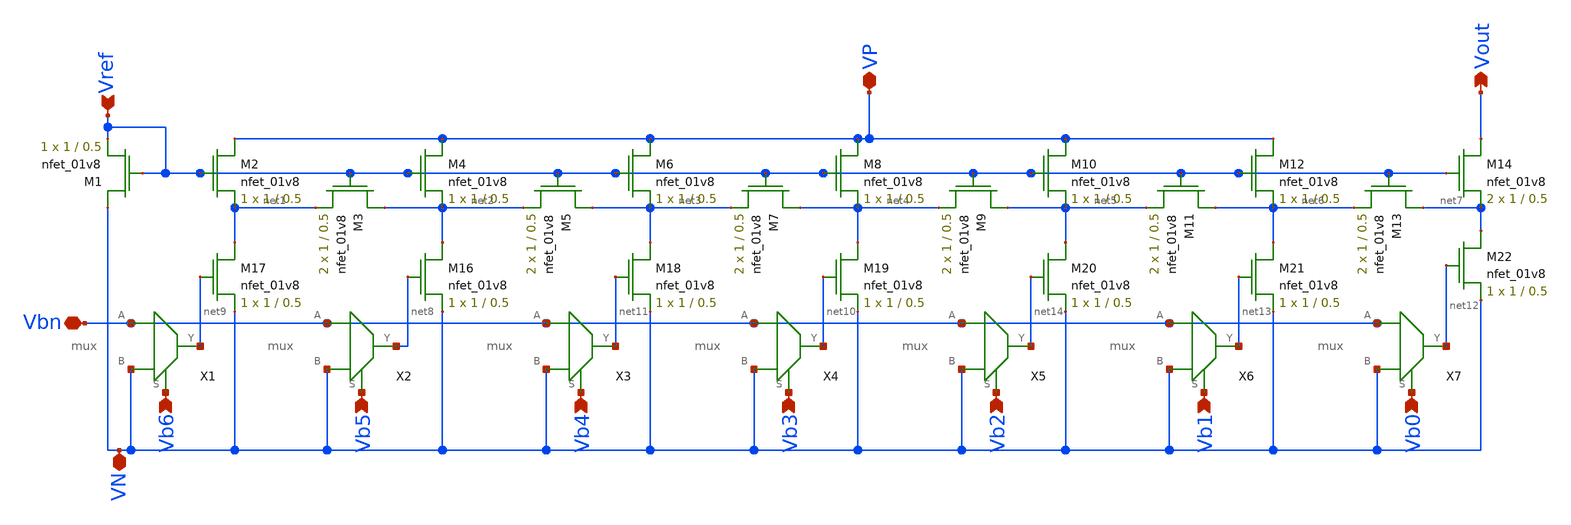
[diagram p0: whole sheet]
** sch_path: dac/schematics/misc/dac.sch
**.subckt dac VN VP Vout Vref Vb6 Vb5 Vb4 Vb3 Vb2 Vb1 Vb0 Vbn
*.iopin VN
*.iopin VP
*.opin Vout
*.ipin Vref
*.ipin Vb6
*.ipin Vb5
*.ipin Vb4
*.ipin Vb3
*.ipin Vb2
*.ipin Vb1
*.ipin Vb0
*.iopin Vbn
XM1 VN Vref Vref GND sky130_fd_pr__nfet_01v8 L=0.5 W=1 nf=1 ad='int((nf+1)/2) * W/nf * 0.29' as='int((nf+2)/2) * W/nf * 0.29'
+ pd='2*int((nf+1)/2) * (W/nf + 0.29)' ps='2*int((nf+2)/2) * (W/nf + 0.29)' nrd='0.29 / W' nrs='0.29 / W'
+ sa=0 sb=0 sd=0 mult=1 m=1
XM3 net2 Vref net1 GND sky130_fd_pr__nfet_01v8 L=0.5 W=1 nf=1 ad='int((nf+1)/2) * W/nf * 0.29' as='int((nf+2)/2) * W/nf * 0.29'
+ pd='2*int((nf+1)/2) * (W/nf + 0.29)' ps='2*int((nf+2)/2) * (W/nf + 0.29)' nrd='0.29 / W' nrs='0.29 / W'
+ sa=0 sb=0 sd=0 mult=2 m=2
XM2 VP Vref net1 GND sky130_fd_pr__nfet_01v8 L=0.5 W=1 nf=1 ad='int((nf+1)/2) * W/nf * 0.29' as='int((nf+2)/2) * W/nf * 0.29'
+ pd='2*int((nf+1)/2) * (W/nf + 0.29)' ps='2*int((nf+2)/2) * (W/nf + 0.29)' nrd='0.29 / W' nrs='0.29 / W'
+ sa=0 sb=0 sd=0 mult=1 m=1
XM4 VP Vref net2 GND sky130_fd_pr__nfet_01v8 L=0.5 W=1 nf=1 ad='int((nf+1)/2) * W/nf * 0.29' as='int((nf+2)/2) * W/nf * 0.29'
+ pd='2*int((nf+1)/2) * (W/nf + 0.29)' ps='2*int((nf+2)/2) * (W/nf + 0.29)' nrd='0.29 / W' nrs='0.29 / W'
+ sa=0 sb=0 sd=0 mult=1 m=1
XM6 VP Vref net3 GND sky130_fd_pr__nfet_01v8 L=0.5 W=1 nf=1 ad='int((nf+1)/2) * W/nf * 0.29' as='int((nf+2)/2) * W/nf * 0.29'
+ pd='2*int((nf+1)/2) * (W/nf + 0.29)' ps='2*int((nf+2)/2) * (W/nf + 0.29)' nrd='0.29 / W' nrs='0.29 / W'
+ sa=0 sb=0 sd=0 mult=1 m=1
XM8 VP Vref net4 GND sky130_fd_pr__nfet_01v8 L=0.5 W=1 nf=1 ad='int((nf+1)/2) * W/nf * 0.29' as='int((nf+2)/2) * W/nf * 0.29'
+ pd='2*int((nf+1)/2) * (W/nf + 0.29)' ps='2*int((nf+2)/2) * (W/nf + 0.29)' nrd='0.29 / W' nrs='0.29 / W'
+ sa=0 sb=0 sd=0 mult=1 m=1
XM10 VP Vref net5 GND sky130_fd_pr__nfet_01v8 L=0.5 W=1 nf=1 ad='int((nf+1)/2) * W/nf * 0.29' as='int((nf+2)/2) * W/nf * 0.29'
+ pd='2*int((nf+1)/2) * (W/nf + 0.29)' ps='2*int((nf+2)/2) * (W/nf + 0.29)' nrd='0.29 / W' nrs='0.29 / W'
+ sa=0 sb=0 sd=0 mult=1 m=1
XM12 VP Vref net6 GND sky130_fd_pr__nfet_01v8 L=0.5 W=1 nf=1 ad='int((nf+1)/2) * W/nf * 0.29' as='int((nf+2)/2) * W/nf * 0.29'
+ pd='2*int((nf+1)/2) * (W/nf + 0.29)' ps='2*int((nf+2)/2) * (W/nf + 0.29)' nrd='0.29 / W' nrs='0.29 / W'
+ sa=0 sb=0 sd=0 mult=1 m=1
XM14 Vout Vref net7 GND sky130_fd_pr__nfet_01v8 L=0.5 W=1 nf=1 ad='int((nf+1)/2) * W/nf * 0.29' as='int((nf+2)/2) * W/nf * 0.29'
+ pd='2*int((nf+1)/2) * (W/nf + 0.29)' ps='2*int((nf+2)/2) * (W/nf + 0.29)' nrd='0.29 / W' nrs='0.29 / W'
+ sa=0 sb=0 sd=0 mult=2 m=2
XM5 net3 Vref net2 GND sky130_fd_pr__nfet_01v8 L=0.5 W=1 nf=1 ad='int((nf+1)/2) * W/nf * 0.29' as='int((nf+2)/2) * W/nf * 0.29'
+ pd='2*int((nf+1)/2) * (W/nf + 0.29)' ps='2*int((nf+2)/2) * (W/nf + 0.29)' nrd='0.29 / W' nrs='0.29 / W'
+ sa=0 sb=0 sd=0 mult=2 m=2
XM7 net4 Vref net3 GND sky130_fd_pr__nfet_01v8 L=0.5 W=1 nf=1 ad='int((nf+1)/2) * W/nf * 0.29' as='int((nf+2)/2) * W/nf * 0.29'
+ pd='2*int((nf+1)/2) * (W/nf + 0.29)' ps='2*int((nf+2)/2) * (W/nf + 0.29)' nrd='0.29 / W' nrs='0.29 / W'
+ sa=0 sb=0 sd=0 mult=2 m=2
XM9 net5 Vref net4 GND sky130_fd_pr__nfet_01v8 L=0.5 W=1 nf=1 ad='int((nf+1)/2) * W/nf * 0.29' as='int((nf+2)/2) * W/nf * 0.29'
+ pd='2*int((nf+1)/2) * (W/nf + 0.29)' ps='2*int((nf+2)/2) * (W/nf + 0.29)' nrd='0.29 / W' nrs='0.29 / W'
+ sa=0 sb=0 sd=0 mult=2 m=2
XM11 net6 Vref net5 GND sky130_fd_pr__nfet_01v8 L=0.5 W=1 nf=1 ad='int((nf+1)/2) * W/nf * 0.29' as='int((nf+2)/2) * W/nf * 0.29'
+ pd='2*int((nf+1)/2) * (W/nf + 0.29)' ps='2*int((nf+2)/2) * (W/nf + 0.29)' nrd='0.29 / W' nrs='0.29 / W'
+ sa=0 sb=0 sd=0 mult=2 m=2
XM13 net7 Vref net6 GND sky130_fd_pr__nfet_01v8 L=0.5 W=1 nf=1 ad='int((nf+1)/2) * W/nf * 0.29' as='int((nf+2)/2) * W/nf * 0.29'
+ pd='2*int((nf+1)/2) * (W/nf + 0.29)' ps='2*int((nf+2)/2) * (W/nf + 0.29)' nrd='0.29 / W' nrs='0.29 / W'
+ sa=0 sb=0 sd=0 mult=2 m=2
XM16 net2 net8 VN GND sky130_fd_pr__nfet_01v8 L=0.5 W=1 nf=1 ad='int((nf+1)/2) * W/nf * 0.29' as='int((nf+2)/2) * W/nf * 0.29'
+ pd='2*int((nf+1)/2) * (W/nf + 0.29)' ps='2*int((nf+2)/2) * (W/nf + 0.29)' nrd='0.29 / W' nrs='0.29 / W'
+ sa=0 sb=0 sd=0 mult=1 m=1
XM17 net1 net9 VN GND sky130_fd_pr__nfet_01v8 L=0.5 W=1 nf=1 ad='int((nf+1)/2) * W/nf * 0.29' as='int((nf+2)/2) * W/nf * 0.29'
+ pd='2*int((nf+1)/2) * (W/nf + 0.29)' ps='2*int((nf+2)/2) * (W/nf + 0.29)' nrd='0.29 / W' nrs='0.29 / W'
+ sa=0 sb=0 sd=0 mult=1 m=1
XM18 net3 net11 VN GND sky130_fd_pr__nfet_01v8 L=0.5 W=1 nf=1 ad='int((nf+1)/2) * W/nf * 0.29' as='int((nf+2)/2) * W/nf * 0.29'
+ pd='2*int((nf+1)/2) * (W/nf + 0.29)' ps='2*int((nf+2)/2) * (W/nf + 0.29)' nrd='0.29 / W' nrs='0.29 / W'
+ sa=0 sb=0 sd=0 mult=1 m=1
XM19 net4 net10 VN GND sky130_fd_pr__nfet_01v8 L=0.5 W=1 nf=1 ad='int((nf+1)/2) * W/nf * 0.29' as='int((nf+2)/2) * W/nf * 0.29'
+ pd='2*int((nf+1)/2) * (W/nf + 0.29)' ps='2*int((nf+2)/2) * (W/nf + 0.29)' nrd='0.29 / W' nrs='0.29 / W'
+ sa=0 sb=0 sd=0 mult=1 m=1
XM20 net5 net14 VN GND sky130_fd_pr__nfet_01v8 L=0.5 W=1 nf=1 ad='int((nf+1)/2) * W/nf * 0.29' as='int((nf+2)/2) * W/nf * 0.29'
+ pd='2*int((nf+1)/2) * (W/nf + 0.29)' ps='2*int((nf+2)/2) * (W/nf + 0.29)' nrd='0.29 / W' nrs='0.29 / W'
+ sa=0 sb=0 sd=0 mult=1 m=1
XM21 net6 net13 VN GND sky130_fd_pr__nfet_01v8 L=0.5 W=1 nf=1 ad='int((nf+1)/2) * W/nf * 0.29' as='int((nf+2)/2) * W/nf * 0.29'
+ pd='2*int((nf+1)/2) * (W/nf + 0.29)' ps='2*int((nf+2)/2) * (W/nf + 0.29)' nrd='0.29 / W' nrs='0.29 / W'
+ sa=0 sb=0 sd=0 mult=1 m=1
XM22 net7 net12 VN GND sky130_fd_pr__nfet_01v8 L=0.5 W=1 nf=1 ad='int((nf+1)/2) * W/nf * 0.29' as='int((nf+2)/2) * W/nf * 0.29'
+ pd='2*int((nf+1)/2) * (W/nf + 0.29)' ps='2*int((nf+2)/2) * (W/nf + 0.29)' nrd='0.29 / W' nrs='0.29 / W'
+ sa=0 sb=0 sd=0 mult=1 m=1
X1 Vbn VN net9 Vb6 mux
X2 Vbn VN net8 Vb5 mux
X3 Vbn VN net11 Vb4 mux
X4 Vbn VN net10 Vb3 mux
X5 Vbn VN net14 Vb2 mux
X6 Vbn VN net13 Vb1 mux
X7 Vbn VN net12 Vb0 mux
**.ends

* expanding   symbol:  /home/madvlsi/current-output-dac-vlsi/schematics/mux.sym # of pins=4
** sym_path: dac/schematics/mux.sym
** sch_path: dac/schematics/mux.sch
.subckt mux A B Y S
*.ipin A
*.ipin B
*.ipin S
*.opin Y
XM1 A S Y VDD sky130_fd_pr__pfet_01v8 L=0.15 W=1 nf=1 ad='int((nf+1)/2) * W/nf * 0.29' as='int((nf+2)/2) * W/nf * 0.29'
+ pd='2*int((nf+1)/2) * (W/nf + 0.29)' ps='2*int((nf+2)/2) * (W/nf + 0.29)' nrd='0.29 / W' nrs='0.29 / W'
+ sa=0 sb=0 sd=0 mult=1 m=1
XM3 net1 S VDD VDD sky130_fd_pr__pfet_01v8 L=0.15 W=1 nf=1 ad='int((nf+1)/2) * W/nf * 0.29' as='int((nf+2)/2) * W/nf * 0.29'
+ pd='2*int((nf+1)/2) * (W/nf + 0.29)' ps='2*int((nf+2)/2) * (W/nf + 0.29)' nrd='0.29 / W' nrs='0.29 / W'
+ sa=0 sb=0 sd=0 mult=1 m=1
XM4 net1 S GND GND sky130_fd_pr__nfet_01v8 L=0.15 W=1 nf=1 ad='int((nf+1)/2) * W/nf * 0.29' as='int((nf+2)/2) * W/nf * 0.29'
+ pd='2*int((nf+1)/2) * (W/nf + 0.29)' ps='2*int((nf+2)/2) * (W/nf + 0.29)' nrd='0.29 / W' nrs='0.29 / W'
+ sa=0 sb=0 sd=0 mult=1 m=1
XM5 A net1 Y GND sky130_fd_pr__nfet_01v8 L=0.15 W=1 nf=1 ad='int((nf+1)/2) * W/nf * 0.29' as='int((nf+2)/2) * W/nf * 0.29'
+ pd='2*int((nf+1)/2) * (W/nf + 0.29)' ps='2*int((nf+2)/2) * (W/nf + 0.29)' nrd='0.29 / W' nrs='0.29 / W'
+ sa=0 sb=0 sd=0 mult=1 m=1
XM2 B net1 Y VDD sky130_fd_pr__pfet_01v8 L=0.15 W=1 nf=1 ad='int((nf+1)/2) * W/nf * 0.29' as='int((nf+2)/2) * W/nf * 0.29'
+ pd='2*int((nf+1)/2) * (W/nf + 0.29)' ps='2*int((nf+2)/2) * (W/nf + 0.29)' nrd='0.29 / W' nrs='0.29 / W'
+ sa=0 sb=0 sd=0 mult=1 m=1
XM6 B S Y GND sky130_fd_pr__nfet_01v8 L=0.15 W=1 nf=1 ad='int((nf+1)/2) * W/nf * 0.29' as='int((nf+2)/2) * W/nf * 0.29'
+ pd='2*int((nf+1)/2) * (W/nf + 0.29)' ps='2*int((nf+2)/2) * (W/nf + 0.29)' nrd='0.29 / W' nrs='0.29 / W'
+ sa=0 sb=0 sd=0 mult=1 m=1
.ends

.GLOBAL VDD
.GLOBAL GND
.end
